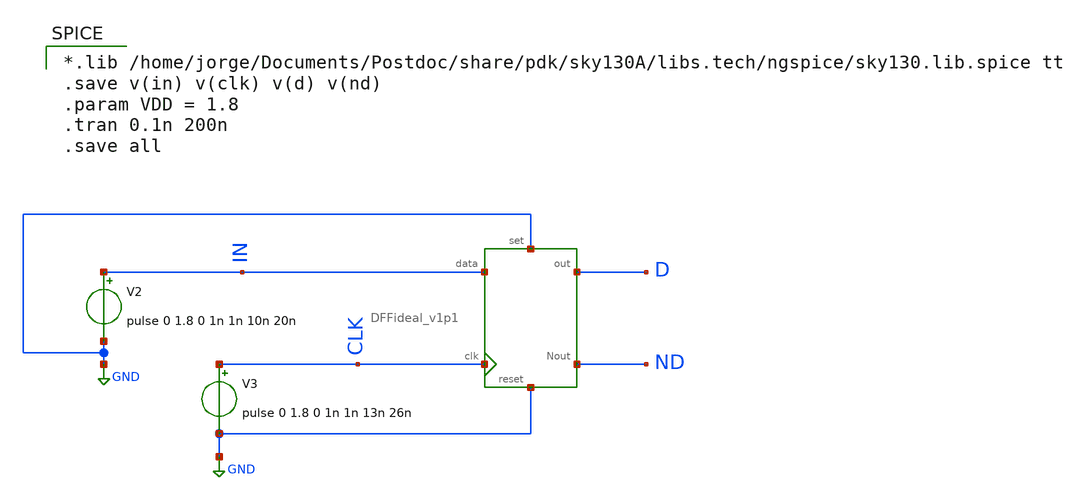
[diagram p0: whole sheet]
** sch_path: xschem/test_DFFideal_v1p1.sch
**.subckt test_DFFideal_v1p1
V2 IN GND pulse 0 1.8 0 1n 1n 10n 20n
V3 CLK GND pulse 0 1.8 0 1n 1n 13n 26n
X1 IN CLK D ND GND GND DFFideal_v1p1
**** begin user architecture code

*.lib /home/jorge/Documents/Postdoc/share/pdk/sky130A/libs.tech/ngspice/sky130.lib.spice tt
.save v(in) v(clk) v(d) v(nd)
.param VDD = 1.8
.tran 0.1n 200n
.save all


**** end user architecture code
**.ends
.GLOBAL GND
**** begin user architecture code
.model flop1 d_dff(clk_delay = 13.0e-9 set_delay = 25.0e-9  reset_delay = 27.0e-9 ic = 2 rise_delay
+ = 10.0e-9  fall_delay = 3e-9)
**** end user architecture code
.end
